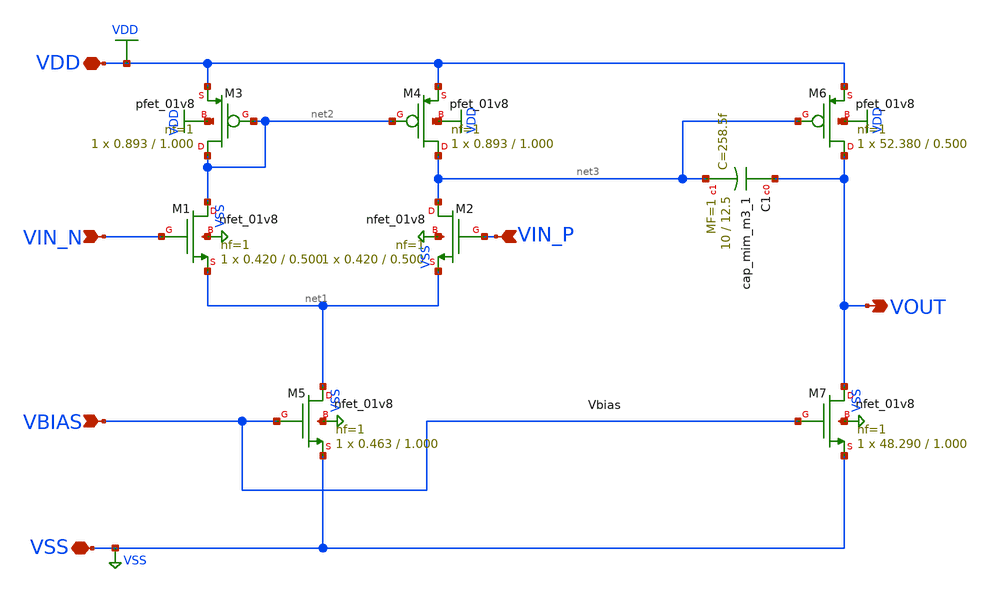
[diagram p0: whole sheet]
** sch_path: analog/bootcamp_opamp/build/schematic/opamp_two_stage.sch
**.subckt opamp_two_stage VIN_P VIN_N VDD VSS VBIAS VOUT
*.ipin VIN_P
*.ipin VIN_N
*.iopin VDD
*.iopin VSS
*.ipin VBIAS
*.opin VOUT
XM1 net2 VIN_N net1 VSS sky130_fd_pr__nfet_01v8 L=0.500 W=0.420 nf=1 ad='int((nf+1)/2) * W/nf * 0.29'
+ as='int((nf+2)/2) * W/nf * 0.29' pd='2*int((nf+1)/2) * (W/nf + 0.29)' ps='2*int((nf+2)/2) * (W/nf + 0.29)'
+ nrd='0.29 / W' nrs='0.29 / W' sa=0 sb=0 sd=0 mult=1 m=1
XM2 net3 VIN_P net1 VSS sky130_fd_pr__nfet_01v8 L=0.500 W=0.420 nf=1 ad='int((nf+1)/2) * W/nf * 0.29'
+ as='int((nf+2)/2) * W/nf * 0.29' pd='2*int((nf+1)/2) * (W/nf + 0.29)' ps='2*int((nf+2)/2) * (W/nf + 0.29)'
+ nrd='0.29 / W' nrs='0.29 / W' sa=0 sb=0 sd=0 mult=1 m=1
XM3 net2 net2 VDD VDD sky130_fd_pr__pfet_01v8 L=1.000 W=0.893 nf=1 ad='int((nf+1)/2) * W/nf * 0.29' as='int((nf+2)/2) * W/nf * 0.29'
+ pd='2*int((nf+1)/2) * (W/nf + 0.29)' ps='2*int((nf+2)/2) * (W/nf + 0.29)' nrd='0.29 / W' nrs='0.29 / W'
+ sa=0 sb=0 sd=0 mult=1 m=1
XM4 net3 net2 VDD VDD sky130_fd_pr__pfet_01v8 L=1.000 W=0.893 nf=1 ad='int((nf+1)/2) * W/nf * 0.29' as='int((nf+2)/2) * W/nf * 0.29'
+ pd='2*int((nf+1)/2) * (W/nf + 0.29)' ps='2*int((nf+2)/2) * (W/nf + 0.29)' nrd='0.29 / W' nrs='0.29 / W'
+ sa=0 sb=0 sd=0 mult=1 m=1
XM5 net1 VBIAS VSS VSS sky130_fd_pr__nfet_01v8 L=1.000 W=0.463 nf=1 ad='int((nf+1)/2) * W/nf * 0.29'
+ as='int((nf+2)/2) * W/nf * 0.29' pd='2*int((nf+1)/2) * (W/nf + 0.29)' ps='2*int((nf+2)/2) * (W/nf + 0.29)'
+ nrd='0.29 / W' nrs='0.29 / W' sa=0 sb=0 sd=0 mult=1 m=1
XM6 VOUT net3 VDD VDD sky130_fd_pr__pfet_01v8 L=0.500 W=52.380 nf=1 ad='int((nf+1)/2) * W/nf * 0.29'
+ as='int((nf+2)/2) * W/nf * 0.29' pd='2*int((nf+1)/2) * (W/nf + 0.29)' ps='2*int((nf+2)/2) * (W/nf + 0.29)'
+ nrd='0.29 / W' nrs='0.29 / W' sa=0 sb=0 sd=0 mult=1 m=1
XC1 VOUT net3 sky130_fd_pr__cap_mim_m3_1 W=10 L=12.5 MF=1 m=1
XM7 VOUT VBIAS VSS VSS sky130_fd_pr__nfet_01v8 L=1.000 W=48.290 nf=1 ad='int((nf+1)/2) * W/nf * 0.29'
+ as='int((nf+2)/2) * W/nf * 0.29' pd='2*int((nf+1)/2) * (W/nf + 0.29)' ps='2*int((nf+2)/2) * (W/nf + 0.29)'
+ nrd='0.29 / W' nrs='0.29 / W' sa=0 sb=0 sd=0 mult=1 m=1
**.ends
.GLOBAL VDD
.GLOBAL VSS
.end
